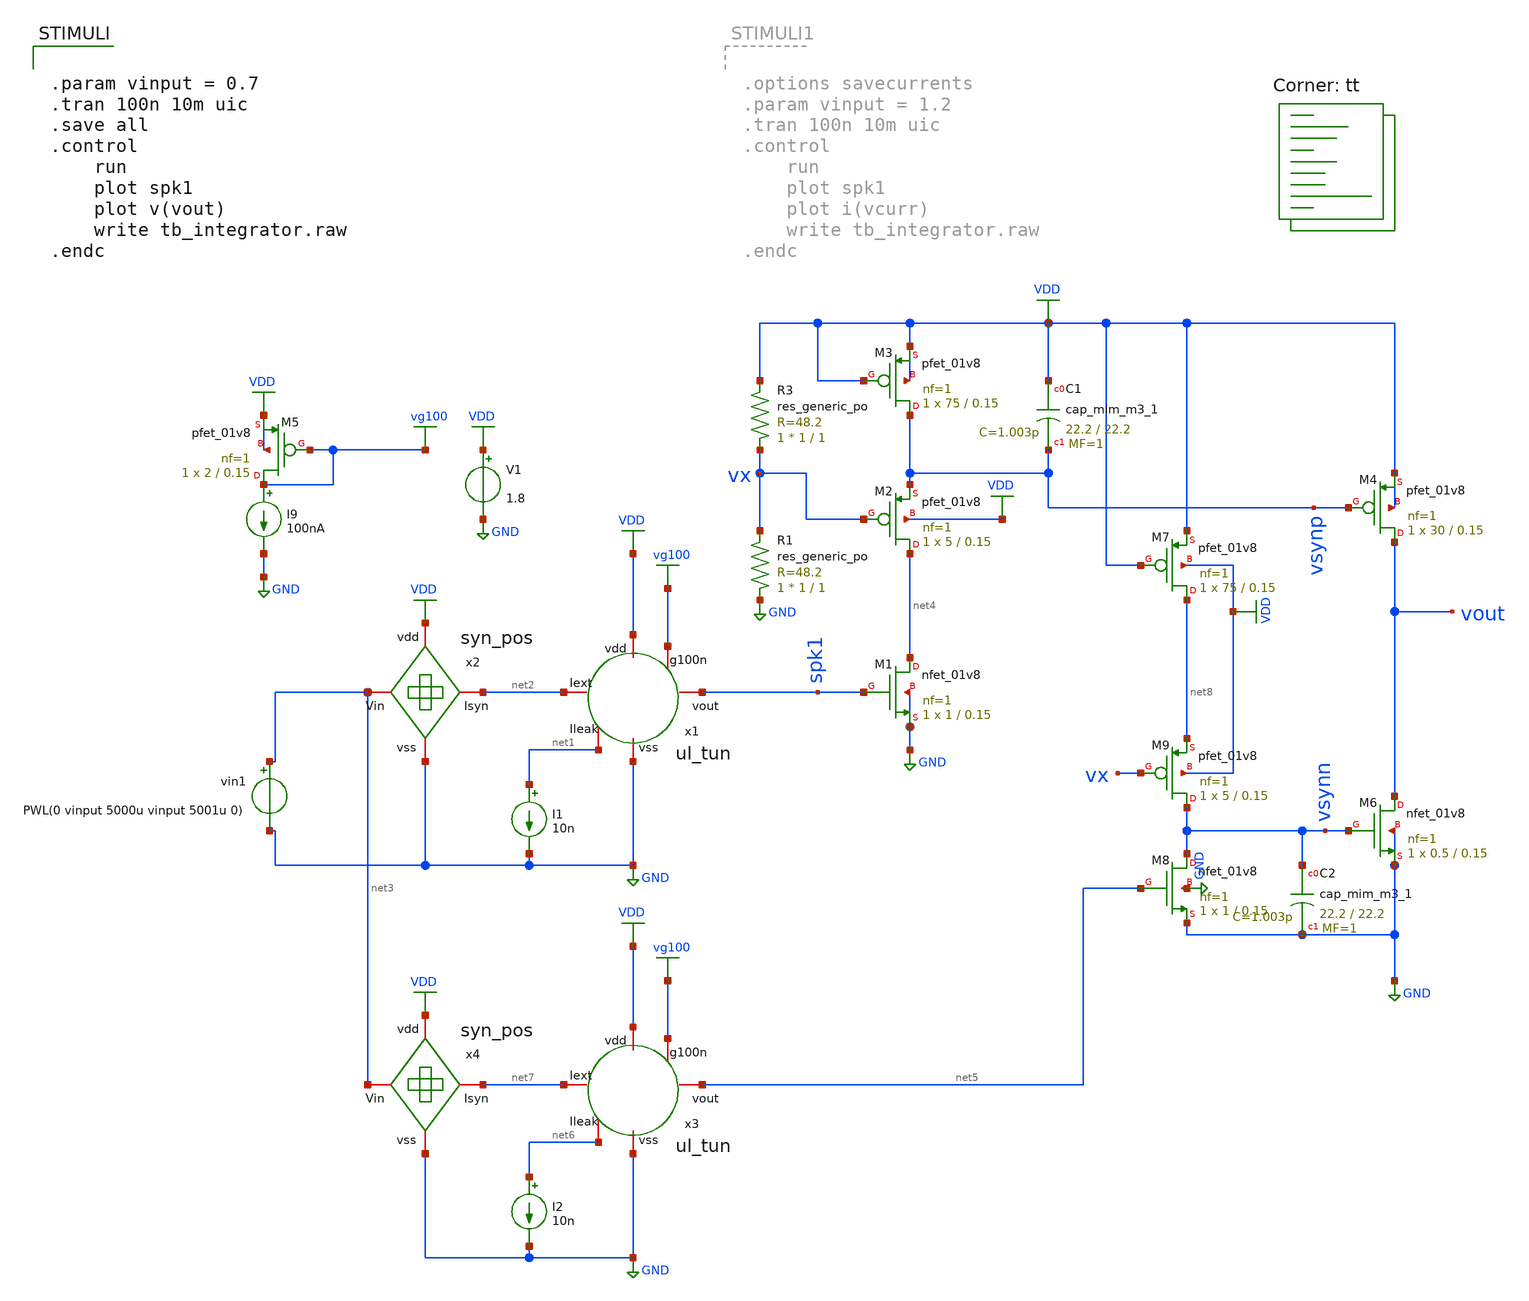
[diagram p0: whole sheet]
** sch_path: Neuron/ultralif/tb_int_pm.sch
**.subckt tb_int_pm
XM1 net4 spk1 GND GND sky130_fd_pr__nfet_01v8 L=0.15 W=1 nf=1 ad='int((nf+1)/2) * W/nf * 0.29' as='int((nf+2)/2) * W/nf * 0.29'
+ pd='2*int((nf+1)/2) * (W/nf + 0.29)' ps='2*int((nf+2)/2) * (W/nf + 0.29)' nrd='0.29 / W' nrs='0.29 / W'
+ sa=0 sb=0 sd=0 mult=1 m=1
XM2 net4 vx vsynp VDD sky130_fd_pr__pfet_01v8 L=0.15 W=5 nf=1 ad='int((nf+1)/2) * W/nf * 0.29' as='int((nf+2)/2) * W/nf * 0.29'
+ pd='2*int((nf+1)/2) * (W/nf + 0.29)' ps='2*int((nf+2)/2) * (W/nf + 0.29)' nrd='0.29 / W' nrs='0.29 / W'
+ sa=0 sb=0 sd=0 mult=1 m=1
XM3 vsynp VDD VDD VDD sky130_fd_pr__pfet_01v8 L=0.15 W=75 nf=1 ad='int((nf+1)/2) * W/nf * 0.29' as='int((nf+2)/2) * W/nf * 0.29'
+ pd='2*int((nf+1)/2) * (W/nf + 0.29)' ps='2*int((nf+2)/2) * (W/nf + 0.29)' nrd='0.29 / W' nrs='0.29 / W'
+ sa=0 sb=0 sd=0 mult=1 m=1
XM4 vout vsynp VDD VDD sky130_fd_pr__pfet_01v8 L=0.15 W=30 nf=1 ad='int((nf+1)/2) * W/nf * 0.29' as='int((nf+2)/2) * W/nf * 0.29'
+ pd='2*int((nf+1)/2) * (W/nf + 0.29)' ps='2*int((nf+2)/2) * (W/nf + 0.29)' nrd='0.29 / W' nrs='0.29 / W'
+ sa=0 sb=0 sd=0 mult=1 m=1
XC1 VDD vsynp sky130_fd_pr__cap_mim_m3_1 W=22.2 L=22.2 MF=1 m=1
V1 VDD GND 1.8
I1 net1 GND 10n
x1 net2 VDD vg100 spk1 net1 GND ul_tun
I9 vg100 GND 100nA
XM5 vg100 vg100 VDD VDD sky130_fd_pr__pfet_01v8 L=0.15 W=2 nf=1 ad='int((nf+1)/2) * W/nf * 0.29' as='int((nf+2)/2) * W/nf * 0.29'
+ pd='2*int((nf+1)/2) * (W/nf + 0.29)' ps='2*int((nf+2)/2) * (W/nf + 0.29)' nrd='0.29 / W' nrs='0.29 / W'
+ sa=0 sb=0 sd=0 mult=1 m=1
vin1 net3 GND PWL(0 vinput 5000u vinput 5001u 0)
x2 VDD net3 net2 GND syn_pos
XR3 vx VDD sky130_fd_pr__res_generic_po W=1 L=1 m=1
XR1 GND vx sky130_fd_pr__res_generic_po W=1 L=1 m=1
XM6 vout vsynn GND GND sky130_fd_pr__nfet_01v8 L=0.15 W=0.5 nf=1 ad='int((nf+1)/2) * W/nf * 0.29' as='int((nf+2)/2) * W/nf * 0.29'
+ pd='2*int((nf+1)/2) * (W/nf + 0.29)' ps='2*int((nf+2)/2) * (W/nf + 0.29)' nrd='0.29 / W' nrs='0.29 / W'
+ sa=0 sb=0 sd=0 mult=1 m=1
I2 net6 GND 10n
x3 net7 VDD vg100 net5 net6 GND ul_tun
XC2 vsynn GND sky130_fd_pr__cap_mim_m3_1 W=22.2 L=22.2 MF=1 m=1
XM7 net8 VDD VDD VDD sky130_fd_pr__pfet_01v8 L=0.15 W=75 nf=1 ad='int((nf+1)/2) * W/nf * 0.29' as='int((nf+2)/2) * W/nf * 0.29'
+ pd='2*int((nf+1)/2) * (W/nf + 0.29)' ps='2*int((nf+2)/2) * (W/nf + 0.29)' nrd='0.29 / W' nrs='0.29 / W'
+ sa=0 sb=0 sd=0 mult=1 m=1
XM8 vsynn net5 GND GND sky130_fd_pr__nfet_01v8 L=0.15 W=1 nf=1 ad='int((nf+1)/2) * W/nf * 0.29' as='int((nf+2)/2) * W/nf * 0.29'
+ pd='2*int((nf+1)/2) * (W/nf + 0.29)' ps='2*int((nf+2)/2) * (W/nf + 0.29)' nrd='0.29 / W' nrs='0.29 / W'
+ sa=0 sb=0 sd=0 mult=1 m=1
XM9 vsynn vx net8 VDD sky130_fd_pr__pfet_01v8 L=0.15 W=5 nf=1 ad='int((nf+1)/2) * W/nf * 0.29' as='int((nf+2)/2) * W/nf * 0.29'
+ pd='2*int((nf+1)/2) * (W/nf + 0.29)' ps='2*int((nf+2)/2) * (W/nf + 0.29)' nrd='0.29 / W' nrs='0.29 / W'
+ sa=0 sb=0 sd=0 mult=1 m=1
x4 VDD net3 net7 GND syn_pos
**** begin user architecture code
.lib $::SKYWATER_MODELS/sky130.lib.spice tt
**** end user architecture code
**.ends

* expanding   symbol:  ul_tun.sym # of pins=6
** sym_path: Neuron/ultralif/ul_tun.sym
** sch_path: Neuron/ultralif/ul_tun.sch
.subckt ul_tun Iext vdd g100n vout Ileak vss
*.iopin Iext
*.iopin vout
*.iopin vss
*.iopin Ileak
*.iopin vdd
*.iopin g100n
XM1 Ileak Ileak net1 vdd sky130_fd_pr__pfet_01v8 L=10 W=1 nf=1 ad='int((nf+1)/2) * W/nf * 0.29' as='int((nf+2)/2) * W/nf * 0.29'
+ pd='2*int((nf+1)/2) * (W/nf + 0.29)' ps='2*int((nf+2)/2) * (W/nf + 0.29)' nrd='0.29 / W' nrs='0.29 / W'
+ sa=0 sb=0 sd=0 mult=1 m=1
XM2 Ileak net2 net1 vdd sky130_fd_pr__pfet_01v8 L=0.15 W=1.5 nf=1 ad='int((nf+1)/2) * W/nf * 0.29' as='int((nf+2)/2) * W/nf * 0.29'
+ pd='2*int((nf+1)/2) * (W/nf + 0.29)' ps='2*int((nf+2)/2) * (W/nf + 0.29)' nrd='0.29 / W' nrs='0.29 / W'
+ sa=0 sb=0 sd=0 mult=1 m=1
XM3 net2 net2 net1 vdd sky130_fd_pr__pfet_01v8 L=0.15 W=15 nf=1 ad='int((nf+1)/2) * W/nf * 0.29' as='int((nf+2)/2) * W/nf * 0.29'
+ pd='2*int((nf+1)/2) * (W/nf + 0.29)' ps='2*int((nf+2)/2) * (W/nf + 0.29)' nrd='0.29 / W' nrs='0.29 / W'
+ sa=0 sb=0 sd=0 mult=1 m=1
XM4 net2 Ileak vss vss sky130_fd_pr__nfet_01v8 L=4 W=1 nf=1 ad='int((1 + 1)/2) * 1 / 1 * 0.29' as='int((1 + 2)/2) * 1 / 1 * 0.29'
+ pd='2*int((1 + 1)/2) * (1 / 1 + 0.29)' ps='2*int((1 + 2)/2) * (1 / 1 + 0.29)' nrd='0.29 / 1 ' nrs='0.29 / 1 '
+ sa=0 sb=0 sd=0 mult=1 m=1
C1 net1 vss 1p m=1
XM5 vout_n Ileak vss vss sky130_fd_pr__nfet_01v8 L=0.15 W=1 nf=1 ad='int((1 + 1)/2) * 1 / 1 * 0.29' as='int((1 + 2)/2) * 1 / 1 * 0.29'
+ pd='2*int((1 + 1)/2) * (1 / 1 + 0.29)' ps='2*int((1 + 2)/2) * (1 / 1 + 0.29)' nrd='0.29 / 1 ' nrs='0.29 / 1 '
+ sa=0 sb=0 sd=0 mult=1 m=1
XM6 vout_n g100n vdd vdd sky130_fd_pr__pfet_01v8 L=0.15 W=2 nf=1 ad='int((nf+1)/2) * W/nf * 0.29' as='int((nf+2)/2) * W/nf * 0.29'
+ pd='2*int((nf+1)/2) * (W/nf + 0.29)' ps='2*int((nf+2)/2) * (W/nf + 0.29)' nrd='0.29 / W' nrs='0.29 / W'
+ sa=0 sb=0 sd=0 mult=1 m=1
XM7 vout vout_n vss vss sky130_fd_pr__nfet_01v8 L=0.15 W=1 nf=1 ad='int((1 + 1)/2) * 1 / 1 * 0.29' as='int((1 + 2)/2) * 1 / 1 * 0.29'
+ pd='2*int((1 + 1)/2) * (1 / 1 + 0.29)' ps='2*int((1 + 2)/2) * (1 / 1 + 0.29)' nrd='0.29 / 1 ' nrs='0.29 / 1 '
+ sa=0 sb=0 sd=0 mult=1 m=1
XM8 vout vout_n vdd vdd sky130_fd_pr__pfet_01v8 L=0.15 W=2 nf=1 ad='int((nf+1)/2) * W/nf * 0.29' as='int((nf+2)/2) * W/nf * 0.29'
+ pd='2*int((nf+1)/2) * (W/nf + 0.29)' ps='2*int((nf+2)/2) * (W/nf + 0.29)' nrd='0.29 / W' nrs='0.29 / W'
+ sa=0 sb=0 sd=0 mult=1 m=1
vext Iext net1 0
**** begin user architecture code


.save i(vext)


**** end user architecture code
.ends


* expanding   symbol:  syn_pos.sym # of pins=4
** sym_path: Neuron/ultralif/syn_pos.sym
** sch_path: Neuron/ultralif/syn_pos.sch
.subckt syn_pos vdd Vin Isyn vss
*.iopin Vin
*.iopin vdd
*.iopin vss
*.iopin Isyn
XM9 Isyn vx vdd vdd sky130_fd_pr__pfet_01v8 L=1 W=0.5 nf=1 ad='int((nf+1)/2) * W/nf * 0.29' as='int((nf+2)/2) * W/nf * 0.29'
+ pd='2*int((nf+1)/2) * (W/nf + 0.29)' ps='2*int((nf+2)/2) * (W/nf + 0.29)' nrd='0.29 / W' nrs='0.29 / W'
+ sa=0 sb=0 sd=0 mult=1 m=1
XM10 vx vx vdd vdd sky130_fd_pr__pfet_01v8 L=0.15 W=0.5 nf=1 ad='int((nf+1)/2) * W/nf * 0.29' as='int((nf+2)/2) * W/nf * 0.29'
+ pd='2*int((nf+1)/2) * (W/nf + 0.29)' ps='2*int((nf+2)/2) * (W/nf + 0.29)' nrd='0.29 / W' nrs='0.29 / W'
+ sa=0 sb=0 sd=0 mult=5 m=5
XM12 vx Vin vss vss sky130_fd_pr__nfet_01v8 L=1 W=0.4 nf=1 ad='int((1 + 1)/2) * 0.4 / 1 * 0.29' as='int((1 + 2)/2) * 0.4 / 1 * 0.29'
+ pd='2*int((1 + 1)/2) * (0.4 / 1 + 0.29)' ps='2*int((1 + 2)/2) * (0.4 / 1 + 0.29)' nrd='0.29 / 0.4 ' nrs='0.29 / 0.4 '
+ sa=0 sb=0 sd=0 mult=1 m=1
.ends

.GLOBAL GND
.GLOBAL VDD
.GLOBAL vg100
**** begin user architecture code


.param vinput = 0.7
.tran 100n 10m uic
.save all
.control
	run
	plot spk1
	plot v(vout)
	write tb_integrator.raw
.endc


**** end user architecture code
.end
